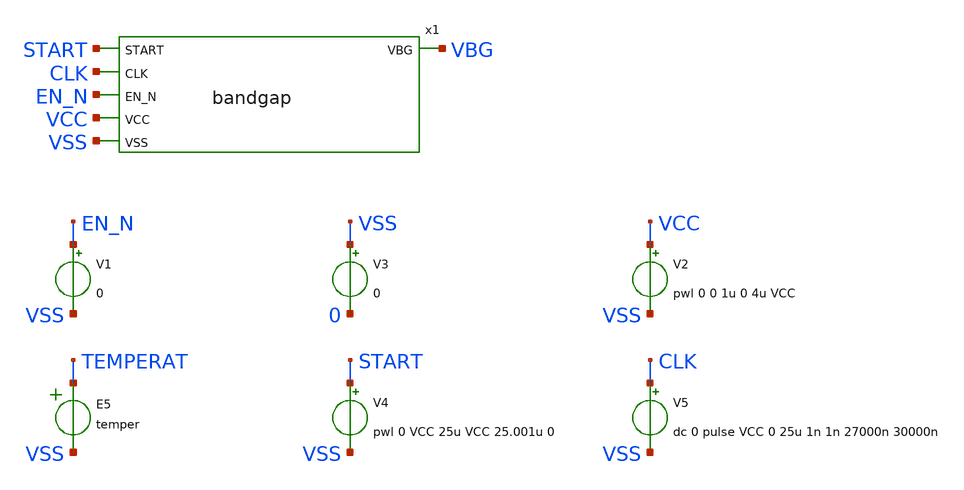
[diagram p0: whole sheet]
** sch_path: xyce/sky130A-xyce/libs.tech/xschem/sky130_tests/tb_bandgap.sch
* Copyright 2020 Stefan Frederik Schippers
* Licensed under the Apache License, Version 2.0 (the "License");
* you may not use this file except in compliance with the License.
* You may obtain a copy of the License at
* https://www.apache.org/licenses/LICENSE-2.0
* Unless required by applicable law or agreed to in writing, software
* distributed under the License is distributed on an "AS IS" BASIS,
* WITHOUT WARRANTIES OR CONDITIONS OF ANY KIND, either express or implied.
* See the License for the specific language governing permissions and
* limitations under the License.
**.subckt tb_bandgap
x1 START CLK EN_N VBG VCC VSS bandgap
V1 EN_N VSS 0
V2 VCC VSS pwl 0 0 1u 0 4u VCC
V3 VSS 0 0
E5 TEMPERAT VSS VOL=' temper '
V4 START VSS pwl 0 VCC 25u VCC 25.001u 0
V5 CLK VSS dc 0 pulse VCC 0 25u 1n 1n 27000n 30000n
**** begin user architecture code

.option seed=13

* this experimental option enables mos model bin
* selection based on W/NF instead of W
.options wnflag=1 XMU=0.49 METHOD=GEAR ITL4=100 CHGTOL=1e-15 TRTOL=1 RELTOL=0.0001 VNTOL=0.1u
.param ABSVAR=0.03
.param VCCGAUSS=agauss(1.8, 'ABSVAR', 1)
.param VCC=VCCGAUSS
* .param VCC=1.8
** variation marameters:
.param sky130_fd_pr__nfet_01v8_lvt__vth0_slope_spectre='agauss(0, ABSVAR, 3)/sky130_fd_pr__nfet_01v8_lvt__vth0_slope'
.param sky130_fd_pr__pfet_01v8_lvt__vth0_slope_spectre='agauss(0, ABSVAR, 3)/sky130_fd_pr__pfet_01v8_lvt__vth0_slope'
.param sky130_fd_pr__nfet_01v8__vth0_slope_spectre='agauss(0, ABSVAR, 3)/sky130_fd_pr__nfet_01v8__vth0_slope'
.param sky130_fd_pr__pfet_01v8__vth0_slope_spectre='agauss(0, ABSVAR, 3)/sky130_fd_pr__pfet_01v8__vth0_slope'

.param sky130_fd_pr__pfet_01v8__toxe_slope_spectre='agauss(0, ABSVAR*2, 3)/sky130_fd_pr__pfet_01v8__toxe_slope'
.param sky130_fd_pr__nfet_01v8__toxe_slope_spectre='agauss(0, ABSVAR*2, 3)/sky130_fd_pr__nfet_01v8__toxe_slope'
.param sky130_fd_pr__pfet_01v8_lvt__toxe_slope_spectre='agauss(0, ABSVAR*2, 3)/sky130_fd_pr__pfet_01v8_lvt__toxe_slope'
.param sky130_fd_pr__nfet_01v8_lvt__toxe_slope_spectre='agauss(0, ABSVAR*2, 3)/sky130_fd_pr__nfet_01v8_lvt__toxe_slope'

.param sky130_fd_pr__res_high_po__var_mult=agauss(0, 'ABSVAR*8', 1)

* .options savecurrents
.control
  let run=1
  dowhile run <= 40
    if run > 1
      reset
      set appendwrite
    end
    * save vbg x1.plus x1.minus i(v2) vcc
    save all
    if run % 3 = 0
      set temp=-40
    end
    if run % 3 = 1
      set temp=27
    end
    if run % 3 = 2
      set temp=125
    end
    tran 0.05u 150u
    write tb_bandgap.raw
    let run = run + 1
  end
  set nolegend
  plot all.vbg
.endc



.include $::SKYWATER_MODELS/cells/nfet_01v8/sky130_fd_pr__nfet_01v8__tt.corner.spice
.include $::SKYWATER_MODELS/cells/nfet_01v8_lvt/sky130_fd_pr__nfet_01v8_lvt__tt.corner.spice
.include $::SKYWATER_MODELS/cells/pfet_01v8/sky130_fd_pr__pfet_01v8__tt.corner.spice
.include $::SKYWATER_MODELS/cells/nfet_03v3_nvt/sky130_fd_pr__nfet_03v3_nvt__tt.corner.spice
.include $::SKYWATER_MODELS/cells/nfet_05v0_nvt/sky130_fd_pr__nfet_05v0_nvt__tt.corner.spice
.include $::SKYWATER_MODELS/cells/esd_nfet_01v8/sky130_fd_pr__esd_nfet_01v8__tt.corner.spice
.include $::SKYWATER_MODELS/cells/pfet_01v8_lvt/sky130_fd_pr__pfet_01v8_lvt__tt.corner.spice
.include $::SKYWATER_MODELS/cells/pfet_01v8_hvt/sky130_fd_pr__pfet_01v8_hvt__tt.corner.spice
.include $::SKYWATER_MODELS/cells/esd_pfet_g5v0d10v5/sky130_fd_pr__esd_pfet_g5v0d10v5__tt.corner.spice
.include $::SKYWATER_MODELS/cells/pfet_g5v0d10v5/sky130_fd_pr__pfet_g5v0d10v5__tt.corner.spice
.include $::SKYWATER_MODELS/cells/pfet_g5v0d16v0/sky130_fd_pr__pfet_g5v0d16v0__tt.corner.spice
.include $::SKYWATER_MODELS/cells/nfet_g5v0d10v5/sky130_fd_pr__nfet_g5v0d10v5__tt.corner.spice
.include $::SKYWATER_MODELS/cells/nfet_g5v0d16v0/sky130_fd_pr__nfet_g5v0d16v0__tt_discrete.corner.spice
.include $::SKYWATER_MODELS/cells/esd_nfet_g5v0d10v5/sky130_fd_pr__esd_nfet_g5v0d10v5__tt.corner.spice
.include $::SKYWATER_MODELS/models/corners/tt/nonfet.spice
* Mismatch parameters
.include $::SKYWATER_MODELS/cells/nfet_01v8/sky130_fd_pr__nfet_01v8__mismatch.corner.spice
.include $::SKYWATER_MODELS/cells/pfet_01v8/sky130_fd_pr__pfet_01v8__mismatch.corner.spice
.include $::SKYWATER_MODELS/cells/nfet_01v8_lvt/sky130_fd_pr__nfet_01v8_lvt__mismatch.corner.spice
.include $::SKYWATER_MODELS/cells/pfet_01v8_lvt/sky130_fd_pr__pfet_01v8_lvt__mismatch.corner.spice
.include $::SKYWATER_MODELS/cells/pfet_01v8_hvt/sky130_fd_pr__pfet_01v8_hvt__mismatch.corner.spice
.include $::SKYWATER_MODELS/cells/nfet_g5v0d10v5/sky130_fd_pr__nfet_g5v0d10v5__mismatch.corner.spice
.include $::SKYWATER_MODELS/cells/pfet_g5v0d10v5/sky130_fd_pr__pfet_g5v0d10v5__mismatch.corner.spice
.include $::SKYWATER_MODELS/cells/nfet_05v0_nvt/sky130_fd_pr__nfet_05v0_nvt__mismatch.corner.spice
.include $::SKYWATER_MODELS/cells/nfet_03v3_nvt/sky130_fd_pr__nfet_03v3_nvt__mismatch.corner.spice
* Resistor$::SKYWATER_MODELS/Capacitor
.include $::SKYWATER_MODELS/models/r+c/res_typical__cap_typical.spice
.include $::SKYWATER_MODELS/models/r+c/res_typical__cap_typical__lin.spice
* Special cells
.include $::SKYWATER_MODELS/models/corners/tt/specialized_cells.spice
* All models
.include $::SKYWATER_MODELS/models/all.spice
* Corner
.include $::SKYWATER_MODELS/models/corners/tt/rf.spice

**** end user architecture code
**.ends

* expanding   symbol:  sky130_tests/bandgap.sym # of pins=6
** sym_path: xyce/sky130A-xyce/libs.tech/xschem/sky130_tests/bandgap.sym
** sch_path: xyce/sky130A-xyce/libs.tech/xschem/sky130_tests/bandgap.sch
.subckt bandgap START CLK EN_N VBG VCC VSS
*.ipin EN_N
*.opin VBG
*.ipin VCC
*.ipin VSS
*.ipin CLK
*.ipin START
XQ1 net7 net2 PLUS VSS sky130_fd_pr__pnp_05v5_W0p68L0p68 m=1
XQ2 net8 net1 E2 VSS sky130_fd_pr__pnp_05v5_W0p68L0p68 m=8
Vc1 net7 VSS 0
.save i(vc1)
Vb1 net2 VSS 0
.save i(vb1)
Vb2 net1 VSS 0
.save i(vb2)
Vc2 net8 VSS 0
.save i(vc2)
x1 EN_N MINUS PLUS VBG VCC VSS ADJ START bandgap_opamp
V1 VBG net9 0
.save i(v1)
V2 VBG net10 0
.save i(v2)
x2 EN_N net3 PLUS net4 VCC VSS ADJ2 zero_opamp
x3 net3 PLUS F2N F2 VCC VSS passgate W_N=0.5 L_N=0.15 W_P=0.5 L_P=0.15 m=1
x4 net3 MINUS F1N F1 VCC VSS passgate W_N=0.5 L_N=0.15 W_P=0.5 L_P=0.15 m=1
x5 ADJ2 net4 F2N F2 VCC VSS passgate W_N=0.5 L_N=0.15 W_P=0.5 L_P=0.15 m=1
x6 ADJ net4 F1N F1 VCC VSS passgate W_N=0.5 L_N=0.15 W_P=0.5 L_P=0.15 m=1
x8 CLK net5 net11 VCC VSS lvnand WidthN=1 LenN=0.15 WidthP=1 LenP=0.15 m=1
x9 net12 net6 net13 VCC VSS lvnand WidthN=1 LenN=0.15 WidthP=1 LenP=0.15 m=1
x10 net12 CLK VCC VSS not W_N=1 L_N=0.15 W_P=2 L_P=0.15 m=1
x11 F2 net6 VCC VSS not W_N=1 L_N=0.15 W_P=2 L_P=0.15 m=1
x12 net14 net11 VCC VSS not W_N=0.5 L_N=1 W_P=1 L_P=1 m=1
x13 net15 net14 VCC VSS not W_N=0.5 L_N=1 W_P=1 L_P=1 m=1
x14 net16 net15 VCC VSS not W_N=0.5 L_N=1 W_P=1 L_P=1 m=1
x15 net6 net16 VCC VSS not W_N=0.5 L_N=1 W_P=1 L_P=1 m=1
x16 net17 net13 VCC VSS not W_N=0.5 L_N=1 W_P=1 L_P=1 m=1
x17 net18 net17 VCC VSS not W_N=0.5 L_N=1 W_P=1 L_P=1 m=1
x18 net19 net18 VCC VSS not W_N=0.5 L_N=1 W_P=1 L_P=1 m=1
x19 net5 net19 VCC VSS not W_N=0.5 L_N=1 W_P=1 L_P=1 m=1
x20 F1 net5 VCC VSS not W_N=1 L_N=0.15 W_P=2 L_P=0.15 m=1
c2 VBG VSS 5p m=1
x7 ADJ ADJ2 START_N START VCC VSS passgate W_N=0.5 L_N=0.15 W_P=0.5 L_P=0.15 m=1
x21 START_N START VCC VSS not W_N=1 L_N=0.15 W_P=2 L_P=0.15 m=1
x22 F1N F1 VCC VSS not W_N=1 L_N=0.15 W_P=2 L_P=0.15 m=1
x23 F2N F2 VCC VSS not W_N=1 L_N=0.15 W_P=2 L_P=0.15 m=1
XC2 ADJ2 VSS sky130_fd_pr__cap_mim_m3_2 W=10 L=10 MF=5 m=5
XC1 ADJ VSS sky130_fd_pr__cap_mim_m3_2 W=10 L=10 MF=20 m=20
XR1 net20 net10 VSS sky130_fd_pr__res_xhigh_po_0p69 W=0.69 L=10 mult=1 m=1
XR2 net21 net20 VSS sky130_fd_pr__res_xhigh_po_0p69 W=0.69 L=10 mult=1 m=1
XR3 net22 net21 VSS sky130_fd_pr__res_xhigh_po_0p69 W=0.69 L=10 mult=1 m=1
XR4 net23 net22 VSS sky130_fd_pr__res_xhigh_po_0p69 W=0.69 L=10 mult=1 m=1
XR5 net24 net23 VSS sky130_fd_pr__res_xhigh_po_0p69 W=0.69 L=10 mult=1 m=1
XR6 net25 net24 VSS sky130_fd_pr__res_xhigh_po_0p69 W=0.69 L=10 mult=1 m=1
XR7 MINUS net25 VSS sky130_fd_pr__res_xhigh_po_0p69 W=0.69 L=10 mult=1 m=1
XR8 net26 net9 VSS sky130_fd_pr__res_xhigh_po_0p69 W=0.69 L=10 mult=1 m=1
XR9 net27 net26 VSS sky130_fd_pr__res_xhigh_po_0p69 W=0.69 L=10 mult=1 m=1
XR10 net28 net27 VSS sky130_fd_pr__res_xhigh_po_0p69 W=0.69 L=10 mult=1 m=1
XR11 net29 net28 VSS sky130_fd_pr__res_xhigh_po_0p69 W=0.69 L=10 mult=1 m=1
XR12 net30 net29 VSS sky130_fd_pr__res_xhigh_po_0p69 W=0.69 L=10 mult=1 m=1
XR13 net31 net30 VSS sky130_fd_pr__res_xhigh_po_0p69 W=0.69 L=10 mult=1 m=1
XR14 PLUS net31 VSS sky130_fd_pr__res_xhigh_po_0p69 W=0.69 L=10 mult=1 m=1
XR15 E2 MINUS VSS sky130_fd_pr__res_xhigh_po_0p69 W=0.69 L=10 mult=1 m=1
.ends


* expanding   symbol:  sky130_tests/bandgap_opamp.sym # of pins=8
** sym_path: xyce/sky130A-xyce/libs.tech/xschem/sky130_tests/bandgap_opamp.sym
** sch_path: xyce/sky130A-xyce/libs.tech/xschem/sky130_tests/bandgap_opamp.sch
.subckt bandgap_opamp EN_N MINUS PLUS DIFFOUT VCC VSS ADJ START
*.ipin PLUS
*.ipin MINUS
*.ipin EN_N
*.ipin VSS
*.ipin VCC
*.opin DIFFOUT
*.ipin ADJ
*.ipin START
C6 G1 0 2f m=1
XM4 net7 EN_N VCC VCC sky130_fd_pr__pfet_01v8 L=6 W=2 nf=1 ad='W * 0.29' as='W * 0.29' pd='W + 2 * 0.29'
+ ps='W + 2 * 0.29' nrd=0 nrs=0 sa=0 sb=0 sd=0 mult=1 m=1
XM18 G2 G1 VSS VSS sky130_fd_pr__nfet_01v8_lvt L=4 W=6 nf=1 ad='W * 0.29' as='W * 0.29' pd='2*(W + 0.29)'
+ ps='2*(W + 0.29)' nrd=0 nrs=0 sa=0 sb=0 sd=0 mult=1 m=1
XM2 G1 G1 VSS VSS sky130_fd_pr__nfet_01v8_lvt L=4 W=6 nf=1 ad='W * 0.29' as='W * 0.29' pd='2*(W + 0.29)'
+ ps='2*(W + 0.29)' nrd=0 nrs=0 sa=0 sb=0 sd=0 mult=1 m=1
XM20 G2 PLUS net8 VCC sky130_fd_pr__pfet_01v8_lvt L=1 W=4 nf=1 ad='W * 0.29' as='W * 0.29' pd='2*(W + 0.29)'
+ ps='2*(W + 0.29)' nrd=0 nrs=0 sa=0 sb=0 sd=0 mult=1 m=1
XM6 G1 MINUS net9 VCC sky130_fd_pr__pfet_01v8_lvt L=1 W=4 nf=1 ad='W * 0.29' as='W * 0.29' pd='2*(W + 0.29)'
+ ps='2*(W + 0.29)' nrd=0 nrs=0 sa=0 sb=0 sd=0 mult=1 m=1
v1 SP net9 0
.save i(v1)
C4 SP 0 2f m=1
C1 G2 0 2f m=1
C5 DIFFOUT 0 4f m=1
XM11 DIFFOUT G2 net1 VSS sky130_fd_pr__nfet_01v8_lvt L=3 W=6 nf=1 ad='W * 0.29' as='W * 0.29' pd='2*(W + 0.29)'
+ ps='2*(W + 0.29)' nrd=0 nrs=0 sa=0 sb=0 sd=0 mult=4 m=4
v2 SP net8 0
.save i(v2)
XM5 G1 DIFFOUT net10 VCC sky130_fd_pr__pfet_01v8_lvt L=1 W=4 nf=1 ad='W * 0.29' as='W * 0.29' pd='2*(W + 0.29)'
+ ps='2*(W + 0.29)' nrd=0 nrs=0 sa=0 sb=0 sd=0 mult=1 m=1
v3 SP net10 0
.save i(v3)
v4 net1 VSS 0
.save i(v4)
v5 VCC net5 0
.save i(v5)
v6 net7 SP 0
.save i(v6)
XM7 DIFFOUT EN_N VSS VSS sky130_fd_pr__nfet_01v8 L=0.15 W=0.5 nf=1 ad='W * 0.29' as='W * 0.29' pd='2*(W + 0.29)'
+ ps='2*(W + 0.29)' nrd=0 nrs=0 sa=0 sb=0 sd=0 mult=3 m=3
XM1 net2 EN_N VCC VCC sky130_fd_pr__pfet_01v8 L=6 W=1 nf=1 ad='W * 0.29' as='W * 0.29' pd='W + 2 * 0.29'
+ ps='W + 2 * 0.29' nrd=0 nrs=0 sa=0 sb=0 sd=0 mult=1 m=1
XM8 net3 ADJ net2 VCC sky130_fd_pr__pfet_01v8_lvt L=1 W=1 nf=1 ad='W * 0.29' as='W * 0.29' pd='W + 2 * 0.29'
+ ps='W + 2 * 0.29' nrd=0 nrs=0 sa=0 sb=0 sd=0 mult=1 m=1
XM9 net3 ADJ net4 VSS sky130_fd_pr__nfet_01v8_lvt L=1 W=0.5 nf=1 ad='W * 0.29' as='W * 0.29' pd='W + 2 * 0.29'
+ ps='W + 2 * 0.29' nrd=0 nrs=0 sa=0 sb=0 sd=0 mult=1 m=1
XM10 net4 VCC VSS VSS sky130_fd_pr__nfet_01v8_lvt L=6 W=0.5 nf=1 ad='W * 0.29' as='W * 0.29' pd='2*(W + 0.29)'
+ ps='2*(W + 0.29)' nrd=0 nrs=0 sa=0 sb=0 sd=0 mult=1 m=1
x1 START_N START VCC VSS not W_N=1 L_N=0.15 W_P=2 L_P=0.15 m=1
x3 G2 net3 START START_N VCC VSS passgate_nlvt W_N=1 L_N=0.35 W_P=1 L_P=0.35 m=1
XM3 DIFFOUT EN_N net5 VCC sky130_fd_pr__pfet_01v8 L=6 W=2 nf=1 ad='W * 0.29' as='W * 0.29' pd='W + 2 * 0.29'
+ ps='W + 2 * 0.29' nrd=0 nrs=0 sa=0 sb=0 sd=0 mult=2 m=2
XC2 net6 G2 sky130_fd_pr__cap_mim_m3_2 W=5 L=5 MF=8 m=8
XR5 net6 DIFFOUT VSS sky130_fd_pr__res_xhigh_po_0p69 W=0.69 L=5 mult=1 m=1
.ends


* expanding   symbol:  sky130_tests/zero_opamp.sym # of pins=7
** sym_path: xyce/sky130A-xyce/libs.tech/xschem/sky130_tests/zero_opamp.sym
** sch_path: xyce/sky130A-xyce/libs.tech/xschem/sky130_tests/zero_opamp.sch
.subckt zero_opamp EN_N MINUS PLUS DIFFOUT VCC VSS ADJ
*.ipin PLUS
*.ipin MINUS
*.ipin EN_N
*.ipin VSS
*.ipin VCC
*.opin DIFFOUT
*.ipin ADJ
C6 G1 0 2f m=1
XM4 net6 EN_N VCC VCC sky130_fd_pr__pfet_01v8 L=8 W=2 nf=1 ad='W * 0.29' as='W * 0.29' pd='W + 2 * 0.29'
+ ps='W + 2 * 0.29' nrd=0 nrs=0 sa=0 sb=0 sd=0 mult=1 m=1
XM18 G2 G2 VSS VSS sky130_fd_pr__nfet_01v8_lvt L=4 W=2 nf=1 ad='W * 0.29' as='W * 0.29' pd='2*(W + 0.29)'
+ ps='2*(W + 0.29)' nrd=0 nrs=0 sa=0 sb=0 sd=0 mult=1 m=1
XM2 G1 G1 VSS VSS sky130_fd_pr__nfet_01v8_lvt L=4 W=2 nf=1 ad='W * 0.29' as='W * 0.29' pd='2*(W + 0.29)'
+ ps='2*(W + 0.29)' nrd=0 nrs=0 sa=0 sb=0 sd=0 mult=1 m=1
XM20 G2 PLUS net7 VCC sky130_fd_pr__pfet_01v8_lvt L=1 W=4 nf=1 ad='W * 0.29' as='W * 0.29' pd='2*(W + 0.29)'
+ ps='2*(W + 0.29)' nrd=0 nrs=0 sa=0 sb=0 sd=0 mult=1 m=1
XM6 G1 MINUS net8 VCC sky130_fd_pr__pfet_01v8_lvt L=1 W=4 nf=1 ad='W * 0.29' as='W * 0.29' pd='2*(W + 0.29)'
+ ps='2*(W + 0.29)' nrd=0 nrs=0 sa=0 sb=0 sd=0 mult=1 m=1
v1 SP net8 0
.save i(v1)
C4 SP 0 2f m=1
C1 G2 0 2f m=1
C5 DIFFOUT 0 4f m=1
XM11 DIFFOUT G2 net1 VSS sky130_fd_pr__nfet_01v8_lvt L=4 W=2 nf=1 ad='W * 0.29' as='W * 0.29' pd='2*(W + 0.29)'
+ ps='2*(W + 0.29)' nrd=0 nrs=0 sa=0 sb=0 sd=0 mult=1 m=1
v2 SP net7 0
.save i(v2)
v4 net1 VSS 0
.save i(v4)
v6 net6 SP 0
.save i(v6)
XM7 DIFFOUT EN_N VSS VSS sky130_fd_pr__nfet_01v8 L=0.15 W=0.5 nf=1 ad='W * 0.29' as='W * 0.29' pd='2*(W + 0.29)'
+ ps='2*(W + 0.29)' nrd=0 nrs=0 sa=0 sb=0 sd=0 mult=3 m=3
XM46 net9 EN_N VCC VCC sky130_fd_pr__pfet_01v8 L=0.15 W=5 nf=1 ad='W * 0.29' as='W * 0.29' pd='W + 2 * 0.29'
+ ps='W + 2 * 0.29' nrd=0 nrs=0 sa=0 sb=0 sd=0 mult=1 m=1
v17 net9 net3 0
.save i(v17)
XM53 net2 G1 VSS VSS sky130_fd_pr__nfet_01v8_lvt L=4 W=2 nf=1 ad='W * 0.29' as='W * 0.29' pd='2*(W + 0.29)'
+ ps='2*(W + 0.29)' nrd=0 nrs=0 sa=0 sb=0 sd=0 mult=1 m=1
XM54 net2 net2 net3 VCC sky130_fd_pr__pfet_01v8_lvt L=4 W=4 nf=1 ad='W * 0.29' as='W * 0.29' pd='2*(W + 0.29)'
+ ps='2*(W + 0.29)' nrd=0 nrs=0 sa=0 sb=0 sd=0 mult=1 m=1
XM55 DIFFOUT net2 net3 VCC sky130_fd_pr__pfet_01v8_lvt L=4 W=4 nf=1 ad='W * 0.29' as='W * 0.29' pd='2*(W + 0.29)'
+ ps='2*(W + 0.29)' nrd=0 nrs=0 sa=0 sb=0 sd=0 mult=1 m=1
XM8 G1 ADJ net4 VCC sky130_fd_pr__pfet_01v8_lvt L=1 W=1 nf=1 ad='W * 0.29' as='W * 0.29' pd='W + 2 * 0.29'
+ ps='W + 2 * 0.29' nrd=0 nrs=0 sa=0 sb=0 sd=0 mult=1 m=1
XM9 G1 ADJ net5 VSS sky130_fd_pr__nfet_01v8_lvt L=1 W=0.5 nf=1 ad='W * 0.29' as='W * 0.29' pd='W + 2 * 0.29'
+ ps='W + 2 * 0.29' nrd=0 nrs=0 sa=0 sb=0 sd=0 mult=1 m=1
XM10 net5 VCC VSS VSS sky130_fd_pr__nfet_01v8_lvt L=8 W=0.5 nf=1 ad='W * 0.29' as='W * 0.29' pd='2*(W + 0.29)'
+ ps='2*(W + 0.29)' nrd=0 nrs=0 sa=0 sb=0 sd=0 mult=1 m=1
XM1 net4 EN_N VCC VCC sky130_fd_pr__pfet_01v8 L=8 W=1 nf=1 ad='W * 0.29' as='W * 0.29' pd='W + 2 * 0.29'
+ ps='W + 2 * 0.29' nrd=0 nrs=0 sa=0 sb=0 sd=0 mult=1 m=1
.ends


* expanding   symbol:  sky130_tests/passgate.sym # of pins=4
** sym_path: xyce/sky130A-xyce/libs.tech/xschem/sky130_tests/passgate.sym
** sch_path: xyce/sky130A-xyce/libs.tech/xschem/sky130_tests/passgate.sch
.subckt passgate Z A GP GN VCCBPIN VSSBPIN  W_N=1 L_N=0.2 W_P=1 L_P=0.2
*.iopin A
*.iopin Z
*.ipin GP
*.ipin GN
XM1 Z GN A VSSBPIN sky130_fd_pr__nfet_01v8 L=L_N W=W_N nf=1 ad='int((nf+1)/2) * W/nf * 0.29' as='int((nf+2)/2) * W/nf * 0.29'
+ pd='2*int((nf+1)/2) * (W/nf + 0.29)' ps='2*int((nf+2)/2) * (W/nf + 0.29)' nrd='0.29 / W' nrs='0.29 / W'
+ sa=0 sb=0 sd=0 mult=1 m=1
XM2 Z GP A VCCBPIN sky130_fd_pr__pfet_01v8 L=L_P W=W_P nf=1 ad='int((nf+1)/2) * W/nf * 0.29' as='int((nf+2)/2) * W/nf * 0.29'
+ pd='2*int((nf+1)/2) * (W/nf + 0.29)' ps='2*int((nf+2)/2) * (W/nf + 0.29)' nrd='0.29 / W' nrs='0.29 / W'
+ sa=0 sb=0 sd=0 mult=1 m=1
.ends


* expanding   symbol:  sky130_tests/lvnand.sym # of pins=3
** sym_path: xyce/sky130A-xyce/libs.tech/xschem/sky130_tests/lvnand.sym
** sch_path: xyce/sky130A-xyce/libs.tech/xschem/sky130_tests/lvnand.sch
.subckt lvnand A B Y VCCPIN VSSPIN  WidthN=1 LenN=0.15 WidthP=1 LenP=0.15
*.ipin A
*.ipin B
*.opin Y
XM1 Y B S VSSPIN sky130_fd_pr__nfet_01v8 L=LenN W=WidthN nf=1 ad='int((nf+1)/2) * W/nf * 0.29' as='int((nf+2)/2) * W/nf * 0.29'
+ pd='2*int((nf+1)/2) * (W/nf + 0.29)' ps='2*int((nf+2)/2) * (W/nf + 0.29)' nrd='0.29 / W' nrs='0.29 / W'
+ sa=0 sb=0 sd=0 mult=1 m=1
XM2 Y A VCCPIN VCCPIN sky130_fd_pr__pfet_01v8 L=LenP W=WidthP nf=1 ad='int((nf+1)/2) * W/nf * 0.29' as='int((nf+2)/2) * W/nf * 0.29'
+ pd='2*int((nf+1)/2) * (W/nf + 0.29)' ps='2*int((nf+2)/2) * (W/nf + 0.29)' nrd='0.29 / W' nrs='0.29 / W'
+ sa=0 sb=0 sd=0 mult=1 m=1
XM3 Y B VCCPIN VCCPIN sky130_fd_pr__pfet_01v8 L=LenP W=WidthP nf=1 ad='int((nf+1)/2) * W/nf * 0.29' as='int((nf+2)/2) * W/nf * 0.29'
+ pd='2*int((nf+1)/2) * (W/nf + 0.29)' ps='2*int((nf+2)/2) * (W/nf + 0.29)' nrd='0.29 / W' nrs='0.29 / W'
+ sa=0 sb=0 sd=0 mult=1 m=1
XM4 S A VSSPIN VSSPIN sky130_fd_pr__nfet_01v8 L=LenN W=WidthN nf=1 ad='int((nf+1)/2) * W/nf * 0.29' as='int((nf+2)/2) * W/nf * 0.29'
+ pd='2*int((nf+1)/2) * (W/nf + 0.29)' ps='2*int((nf+2)/2) * (W/nf + 0.29)' nrd='0.29 / W' nrs='0.29 / W'
+ sa=0 sb=0 sd=0 mult=1 m=1
.ends


* expanding   symbol:  sky130_tests/not.sym # of pins=2
** sym_path: xyce/sky130A-xyce/libs.tech/xschem/sky130_tests/not.sym
** sch_path: xyce/sky130A-xyce/libs.tech/xschem/sky130_tests/not.sch
.subckt not y a VCCPIN VSSPIN     W_N=1 L_N=0.15 W_P=2 L_P=0.15
*.opin y
*.ipin a
XM1 y a VSSPIN VSSPIN sky130_fd_pr__nfet_01v8 L=L_N W=W_N nf=1 ad='int((nf+1)/2) * W/nf * 0.29' as='int((nf+2)/2) * W/nf * 0.29'
+ pd='2*int((nf+1)/2) * (W/nf + 0.29)' ps='2*int((nf+2)/2) * (W/nf + 0.29)' nrd='0.29 / W' nrs='0.29 / W'
+ sa=0 sb=0 sd=0 mult=1 m=1
XM2 y a VCCPIN VCCPIN sky130_fd_pr__pfet_01v8 L=L_P W=W_P nf=1 ad='int((nf+1)/2) * W/nf * 0.29' as='int((nf+2)/2) * W/nf * 0.29'
+ pd='2*int((nf+1)/2) * (W/nf + 0.29)' ps='2*int((nf+2)/2) * (W/nf + 0.29)' nrd='0.29 / W' nrs='0.29 / W'
+ sa=0 sb=0 sd=0 mult=1 m=1
.ends


* expanding   symbol:  sky130_tests/passgate_nlvt.sym # of pins=4
** sym_path: xyce/sky130A-xyce/libs.tech/xschem/sky130_tests/passgate_nlvt.sym
** sch_path: xyce/sky130A-xyce/libs.tech/xschem/sky130_tests/passgate_nlvt.sch
.subckt passgate_nlvt Z A GP GN VCCBPIN VSSBPIN  W_N=1 L_N=0.35 W_P=1 L_P=0.35
*.iopin A
*.iopin Z
*.ipin GP
*.ipin GN
XM1 Z GN A VSSBPIN sky130_fd_pr__nfet_01v8_lvt L=L_N W=W_N nf=1 ad='int((nf+1)/2) * W/nf * 0.29' as='int((nf+2)/2) * W/nf * 0.29'
+ pd='2*int((nf+1)/2) * (W/nf + 0.29)' ps='2*int((nf+2)/2) * (W/nf + 0.29)' nrd='0.29 / W' nrs='0.29 / W'
+ sa=0 sb=0 sd=0 mult=1 m=1
XM2 Z GP A VCCBPIN sky130_fd_pr__pfet_01v8_lvt L=L_P W=W_P nf=1 ad='int((nf+1)/2) * W/nf * 0.29' as='int((nf+2)/2) * W/nf * 0.29'
+ pd='2*int((nf+1)/2) * (W/nf + 0.29)' ps='2*int((nf+2)/2) * (W/nf + 0.29)' nrd='0.29 / W' nrs='0.29 / W'
+ sa=0 sb=0 sd=0 mult=1 m=1
.ends

.end
